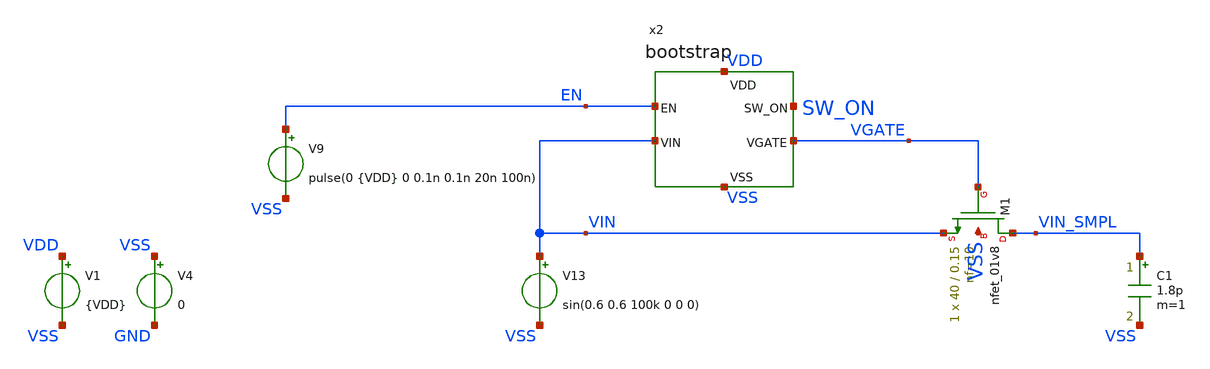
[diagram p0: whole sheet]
** sch_path: simulations/bootstrap_sim.sch

* Skywater 130 nm PDK models
.lib $::SKYWATER_MODELS/sky130.lib.spice tt

* Models for standard digital cells
.include $::SKYWATER_STDCELLS/sky130_fd_sc_hd.spice

**.subckt bootstrap_sim
V1 VDD VSS {VDD}
.save i(v1)
V4 VSS GND 0
V9 EN VSS pulse(0 {VDD} 0 0.1n 0.1n 20n 100n)
x2 VDD VSS VIN SW_ON EN VGATE bootstrap
XM1 VIN_SMPL VGATE VIN VSS sky130_fd_pr__nfet_01v8 L=0.15 W=40 nf=10 ad='int((nf+1)/2) * W/nf * 0.29'
+ as='int((nf+2)/2) * W/nf * 0.29' pd='2*int((nf+1)/2) * (W/nf + 0.29)' ps='2*int((nf+2)/2) * (W/nf + 0.29)'
+ nrd='0.29 / W' nrs='0.29 / W' sa=0 sb=0 sd=0 mult=1 m=1
C1 VIN_SMPL VSS 1.8p m=1
V13 VIN VSS sin(0.6 0.6 100k 0 0 0)
**** begin user architecture code


.param VDD = 1.8
.option temp = 27
.save all

.option GMIN=1e-12 reltol=1e-6
.control
		set ngbehavior=hsa
          		set skywaterpdk
          		set ng_nomodcheck
          		set num_threads=4
          		option noinit
          		option klu
		tran 10n 10u
		write bootstrap_sim.raw
.endc


**** end user architecture code
**.ends

* expanding   symbol:  subcells/bootstrap/bootstrap.sym # of pins=6
** sym_path: bootstrap/bootstrap.sym
** sch_path: bootstrap/bootstrap.sch
.subckt bootstrap VDD VSS VIN SW_ON EN VGATE
*.ipin VDD
*.ipin VSS
*.ipin VIN
*.opin VGATE
*.ipin EN
*.opin SW_ON
XM1 VDD VGATE Vtop Vtop sky130_fd_pr__pfet_01v8 L=0.15 W=1 nf=1 ad='int((nf+1)/2) * W/nf * 0.29' as='int((nf+2)/2) * W/nf * 0.29'
+ pd='2*int((nf+1)/2) * (W/nf + 0.29)' ps='2*int((nf+2)/2) * (W/nf + 0.29)' nrd='0.29 / W' nrs='0.29 / W'
+ sa=0 sb=0 sd=0 mult=1 m=1
XM2 VGATE EN_Z Vtop Vtop sky130_fd_pr__pfet_01v8 L=0.15 W=16 nf=4 ad='int((nf+1)/2) * W/nf * 0.29' as='int((nf+2)/2) * W/nf * 0.29'
+ pd='2*int((nf+1)/2) * (W/nf + 0.29)' ps='2*int((nf+2)/2) * (W/nf + 0.29)' nrd='0.29 / W' nrs='0.29 / W'
+ sa=0 sb=0 sd=0 mult=1 m=1
XM3 VGATE VDD Vd VSS sky130_fd_pr__nfet_05v0_nvt L=0.9 W=8 nf=2 ad='int((nf+1)/2) * W/nf * 0.29' as='int((nf+2)/2) * W/nf * 0.29'
+ pd='2*int((nf+1)/2) * (W/nf + 0.29)' ps='2*int((nf+2)/2) * (W/nf + 0.29)' nrd='0.29 / W' nrs='0.29 / W'
+ sa=0 sb=0 sd=0 mult=1 m=1
XM4 Vd EN_Z VSS VSS sky130_fd_pr__nfet_01v8 L=0.15 W=8 nf=2 ad='int((nf+1)/2) * W/nf * 0.29' as='int((nf+2)/2) * W/nf * 0.29'
+ pd='2*int((nf+1)/2) * (W/nf + 0.29)' ps='2*int((nf+2)/2) * (W/nf + 0.29)' nrd='0.29 / W' nrs='0.29 / W'
+ sa=0 sb=0 sd=0 mult=1 m=1
XM5 Vbottom EN_Z VSS VSS sky130_fd_pr__nfet_01v8 L=0.15 W=8 nf=2 ad='int((nf+1)/2) * W/nf * 0.29' as='int((nf+2)/2) * W/nf * 0.29'
+ pd='2*int((nf+1)/2) * (W/nf + 0.29)' ps='2*int((nf+2)/2) * (W/nf + 0.29)' nrd='0.29 / W' nrs='0.29 / W'
+ sa=0 sb=0 sd=0 mult=1 m=1
XM6 Vtop Vbottom Vtop Vtop sky130_fd_pr__pfet_01v8 L=15 W=15 nf=4 ad='int((nf+1)/2) * W/nf * 0.29' as='int((nf+2)/2) * W/nf * 0.29'
+ pd='2*int((nf+1)/2) * (W/nf + 0.29)' ps='2*int((nf+2)/2) * (W/nf + 0.29)' nrd='0.29 / W' nrs='0.29 / W'
+ sa=0 sb=0 sd=0 mult=1 m=1
x1 EN VSS VSS VDD VDD EN_Z sky130_fd_sc_hd__inv_4
XM8 VIN VGATE Vbottom VSS sky130_fd_pr__nfet_01v8 L=0.15 W=8 nf=2 ad='int((nf+1)/2) * W/nf * 0.29' as='int((nf+2)/2) * W/nf * 0.29'
+ pd='2*int((nf+1)/2) * (W/nf + 0.29)' ps='2*int((nf+2)/2) * (W/nf + 0.29)' nrd='0.29 / W' nrs='0.29 / W'
+ sa=0 sb=0 sd=0 mult=1 m=1
XM7 VGATE VDD VGATE_1V8 VSS sky130_fd_pr__nfet_05v0_nvt L=0.9 W=4 nf=1 ad='int((nf+1)/2) * W/nf * 0.29'
+ as='int((nf+2)/2) * W/nf * 0.29' pd='2*int((nf+1)/2) * (W/nf + 0.29)' ps='2*int((nf+2)/2) * (W/nf + 0.29)'
+ nrd='0.29 / W' nrs='0.29 / W' sa=0 sb=0 sd=0 mult=1 m=1
x2 VGATE_1V8 VSS VSS VDD VDD net1 sky130_fd_sc_hd__inv_2
x3 net1 VSS VSS VDD VDD SW_ON sky130_fd_sc_hd__inv_4
.ends

.end
